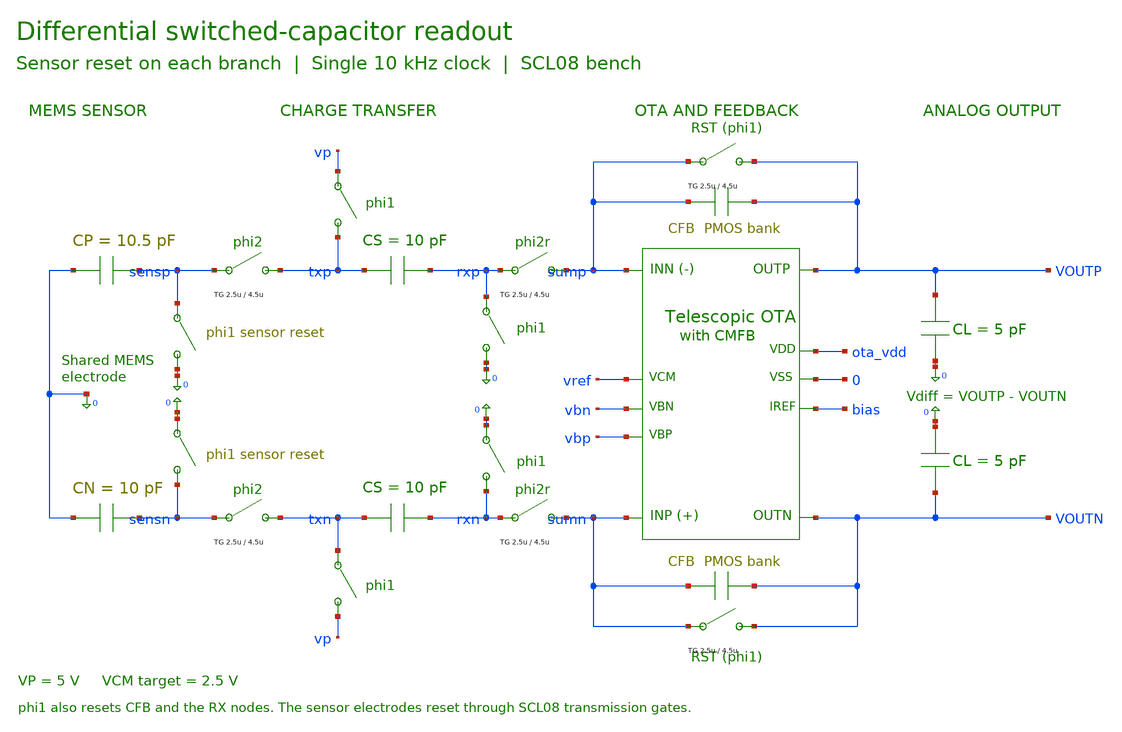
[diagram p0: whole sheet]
** sch_path: OTA/final_design/sc_integration/integrated_sc_ota/sc_ota_integrated.sch
**.subckt sc_ota_integrated
XOTA sumn sump outp outn ota_vdd 0 bias vref vbn vbp ota_core
CMEMP 0 sensp 10.5p
XSENSEP phi2 0 sensp txp vdd phi2b Transmission_v1_26
XSRESETP sensp 0 phi1 phi1b vdd 0 corrected_tg
XCHARGEP vp txp phi1 phi1b vdd 0 corrected_tg
CSP txp rxp 10p
XRRESETP rxp 0 phi1 phi1b vdd 0 corrected_tg
XXFERP phit 0 rxp sump vdd phitb Transmission_v1_26
XCFP sump outp corrected_pmos_bank
XFBRESETP phi1 0 sump outp vdd phi1b Transmission_v1_26
CLP outp 0 5p
CMEMN 0 sensn 10p
XSENSEN phi2 0 sensn txn vdd phi2b Transmission_v1_26
XSRESETN 0 sensn phi1 phi1b vdd 0 corrected_tg
XCHARGEN txn vp phi1 phi1b vdd 0 corrected_tg
CSN txn rxn 10p
XRRESETN 0 rxn phi1 phi1b vdd 0 corrected_tg
XXFERN phit 0 rxn sumn vdd phitb Transmission_v1_26
XCFN sumn outn corrected_pmos_bank
XFBRESETN phi1 0 sumn outn vdd phi1b Transmission_v1_26
CLN 0 outn 5p
**** begin user architecture code
.include bench_support_schematic.spice
**** end user architecture code
**.ends

* expanding   symbol:  ota_core.sym # of pins=10
** sym_path: OTA/final_design/sc_integration/integrated_sc_ota/ota_core.sym
** sch_path: OTA/final_design/sc_integration/integrated_sc_ota/ota_core.sch
.subckt ota_core INP INN OUTP OUTM VDD VSS IREF VCM VBN VBP
*.iopin INP
*.iopin INN
*.iopin OUTP
*.iopin OUTM
*.iopin VDD
*.iopin VSS
*.iopin IREF
*.iopin VCM
*.iopin VBN
*.iopin VBP
MP1 PX1 PC VDD VDD P w=40u l=3.2u AD=180p AS=180p PD=89u PS=89u m=1
MPC1 OUTM VBP PX1 VDD P w=60u l=2.4u AD=270p AS=270p PD=129u PS=129u m=1
MNC1 OUTM VBN NX1 VSS N w=30u l=2.4u AD=135p AS=135p PD=69u PS=69u m=1
MN1 NX1 INP TAIL VSS N w=15u l=2.4u AD=67.5p AS=67.5p PD=39u PS=39u m=1
MP2 PX2 PC VDD VDD P w=40u l=3.2u AD=180p AS=180p PD=89u PS=89u m=1
MPC2 OUTP VBP PX2 VDD P w=60u l=2.4u AD=270p AS=270p PD=129u PS=129u m=1
MNC2 OUTP VBN NX2 VSS N w=30u l=2.4u AD=135p AS=135p PD=69u PS=69u m=1
MN2 NX2 INN TAIL VSS N w=15u l=2.4u AD=67.5p AS=67.5p PD=39u PS=39u m=1
MTAIL TAIL IREF VSS VSS N w=80.0u l=3.2u AD=360p AS=360p PD=169u PS=169u m=1
MREF IREF IREF VSS VSS N w=20u l=3.2u AD=90p AS=90p PD=49u PS=49u m=1
MSP VDD OUTP SP VSS N w=20u l=1.6u AD=90p AS=90p PD=49u PS=49u m=4
MSIP SP IREF VSS VSS N w=20u l=3.2u AD=90p AS=90p PD=49u PS=49u m=2
MSM VDD OUTM SM VSS N w=20u l=1.6u AD=90p AS=90p PD=49u PS=49u m=4
MSIM SM IREF VSS VSS N w=20u l=3.2u AD=90p AS=90p PD=49u PS=49u m=2
MSR VDD VCM SR VSS N w=20u l=1.6u AD=90p AS=90p PD=49u PS=49u m=4
MSIR SR IREF VSS VSS N w=20u l=3.2u AD=90p AS=90p PD=49u PS=49u m=2
XSP SP SENSE RPP W=2.4u L=17142.857143u
XSM SM SENSE RPP W=2.4u L=17142.857143u
MCT CT CB VDD VDD P w=10u l=3.2u AD=45p AS=45p PD=29u PS=29u m=1
MCBI CB CB VDD VDD P w=20u l=3.2u AD=90p AS=90p PD=49u PS=49u m=1
MCBN CB IREF VSS VSS N w=11.428571u l=3.2u AD=51.4286p AS=51.4286p PD=31.8571u PS=31.8571u m=1
MCS CA SENSE CT VDD P w=5u l=2.4u AD=22.5p AS=22.5p PD=19u PS=19u m=1
MCR RCM SR CT VDD P w=5u l=2.4u AD=22.5p AS=22.5p PD=19u PS=19u m=1
MCFN1 CA CA VSS VSS N w=10u l=3.2u AD=45p AS=45p PD=29u PS=29u m=1
MCFN3 RCM RCM VSS VSS N w=10u l=3.2u AD=45p AS=45p PD=29u PS=29u m=1
MCFP1 PBIAS PBIAS VDD VDD P w=10u l=3.2u AD=45p AS=45p PD=29u PS=29u m=1
MCFN4 PBIAS RCM VSS VSS N w=10u l=3.2u AD=45p AS=45p PD=29u PS=29u m=1
MCFP2 PC PBIAS VDD VDD P w=10u l=3.2u AD=45p AS=45p PD=29u PS=29u m=1
MCFN2 PC CA VSS VSS N w=10u l=3.2u AD=45p AS=45p PD=29u PS=29u m=1
MCC VDD PC VDD VDD P w=20u l=10u AD=90p AS=90p PD=49u PS=49u m=4
MCM1 OUTP PC OUTP OUTP P w=20u l=10u AD=90p AS=90p PD=49u PS=49u m=12
MCM2 OUTM PC OUTM OUTM P w=20u l=10u AD=90p AS=90p PD=49u PS=49u m=12
.ends

.end
